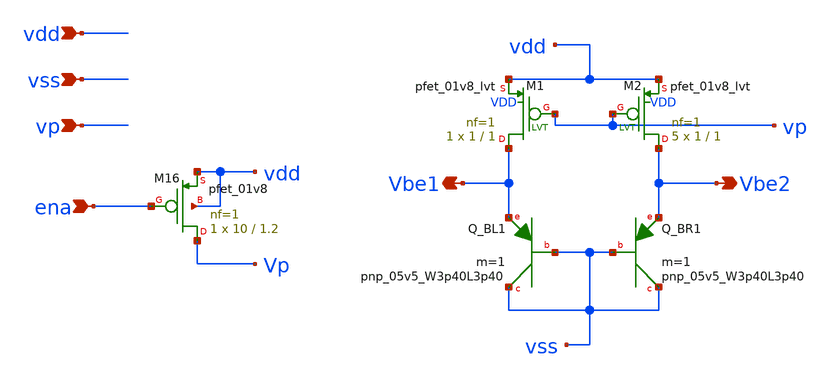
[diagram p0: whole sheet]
** sch_path: xschem/sky130_od_ip__tempsensor_ext_vp.sch
**.subckt sky130_od_ip__tempsensor_ext_vp vdd vss Vbe2 Vbe1 ena vp
*.ipin vdd
*.ipin vss
*.opin Vbe2
*.opin Vbe1
*.ipin ena
*.ipin vp
XQ_BL1 vss vss Vbe1 sky130_fd_pr__pnp_05v5_W3p40L3p40 m=1
XQ_BR1 vss vss Vbe2 sky130_fd_pr__pnp_05v5_W3p40L3p40 m=1
XM16 Vp ena vdd vdd sky130_fd_pr__pfet_01v8 L=1.2 W=10 nf=1 ad='int((nf+1)/2) * W/nf * 0.29' as='int((nf+2)/2) * W/nf * 0.29'
+ pd='2*int((nf+1)/2) * (W/nf + 0.29)' ps='2*int((nf+2)/2) * (W/nf + 0.29)' nrd='0.29 / W' nrs='0.29 / W'
+ sa=0 sb=0 sd=0 mult=1 m=1
XM1 Vbe1 vp vdd VDD sky130_fd_pr__pfet_01v8_lvt L=1 W=1 nf=1 ad='int((nf+1)/2) * W/nf * 0.29' as='int((nf+2)/2) * W/nf * 0.29'
+ pd='2*int((nf+1)/2) * (W/nf + 0.29)' ps='2*int((nf+2)/2) * (W/nf + 0.29)' nrd='0.29 / W' nrs='0.29 / W'
+ sa=0 sb=0 sd=0 mult=1 m=1
XM2 Vbe2 vp vdd VDD sky130_fd_pr__pfet_01v8_lvt L=1 W=1 nf=1 ad='int((nf+1)/2) * W/nf * 0.29' as='int((nf+2)/2) * W/nf * 0.29'
+ pd='2*int((nf+1)/2) * (W/nf + 0.29)' ps='2*int((nf+2)/2) * (W/nf + 0.29)' nrd='0.29 / W' nrs='0.29 / W'
+ sa=0 sb=0 sd=0 mult=5 m=5
**.ends
.end
